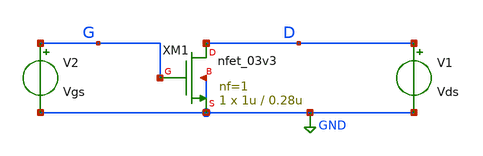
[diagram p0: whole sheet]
** sch_path: gf180mcuD/xschem_libs/gf180mcu_tests/test_nfet_final/schematic/test_nfet_final.sch
**.subckt test_nfet_final
XM1 D G GND GND nfet_03v3 L=0.28u W=1u nf=1 ad='int((nf+1)/2) * W/nf * 0.18u' as='int((nf+2)/2) * W/nf * 0.18u'
+ pd='2*int((nf+1)/2) * (W/nf + 0.18u)' ps='2*int((nf+2)/2) * (W/nf + 0.18u)' nrd='0.18u / W' nrs='0.18u / W'
+ sa=0 sb=0 sd=0 m=1
V1 D GND Vds
V2 G GND Vgs
**.ends
.GLOBAL GND
.end
